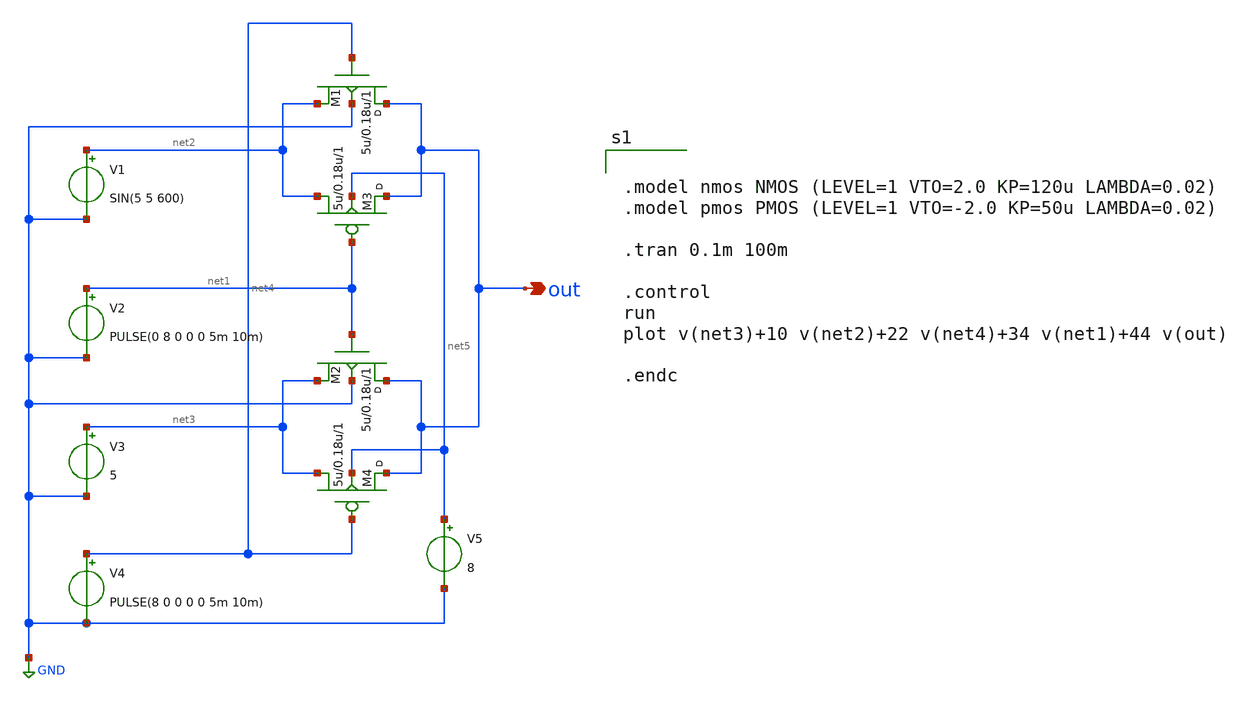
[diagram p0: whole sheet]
** sch_path: analog_mux_ask.sch
**.subckt analog_mux_ask out
*.opin out
V1 net2 GND SIN(5 5 600)
V2 net1 GND PULSE(0 8 0 0 0 5m 10m)
V3 net3 GND 5
V4 net4 GND PULSE(8 0 0 0 0 5m 10m)
M1 out net4 net2 GND nmos w=5u l=0.18u m=1
M2 out net1 net3 GND nmos w=5u l=0.18u m=1
M3 out net1 net2 net5 pmos w=5u l=0.18u m=1
M4 out net4 net3 net5 pmos w=5u l=0.18u m=1
V5 net5 GND 8
**** begin user architecture code


.model nmos NMOS (LEVEL=1 VTO=2.0 KP=120u LAMBDA=0.02)
.model pmos PMOS (LEVEL=1 VTO=-2.0 KP=50u LAMBDA=0.02)

.tran 0.1m 100m

.control
run
plot v(net3)+10 v(net2)+22 v(net4)+34 v(net1)+44 v(out)

.endc


**** end user architecture code
**.ends
.GLOBAL GND
.end
